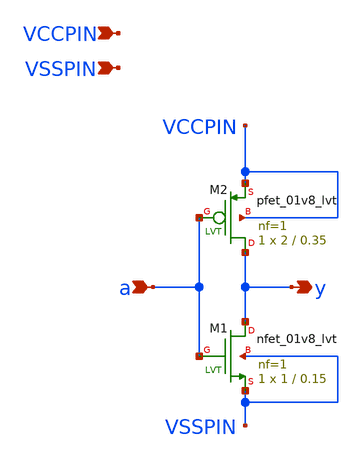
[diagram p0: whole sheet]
** sch_path: xschem/lvtnot.sch
**.subckt lvtnot y a VCCPIN VSSPIN
*.opin y
*.ipin a
*.ipin VCCPIN
*.ipin VSSPIN
XM2 y a VCCPIN VCCPIN sky130_fd_pr__pfet_01v8_lvt L=0.35 W=2 nf=1 ad='int((1 + 1)/2) * 2 / 1 * 0.29'
+ as='int((1 + 2)/2) * 2 / 1 * 0.29' pd='2*int((1 + 1)/2) * (2 / 1 + 0.29)' ps='2*int((1 + 2)/2) * (2 / 1 + 0.29)'
+ nrd='0.29 / 2 ' nrs='0.29 / 2 ' sa=0 sb=0 sd=0 mult=1 m=1
XM1 y a VSSPIN VSSPIN sky130_fd_pr__nfet_01v8_lvt L=0.15 W=1 nf=1 ad='int((1 + 1)/2) * 1 / 1 * 0.29'
+ as='int((1 + 2)/2) * 1 / 1 * 0.29' pd='2*int((1 + 1)/2) * (1 / 1 + 0.29)' ps='2*int((1 + 2)/2) * (1 / 1 + 0.29)'
+ nrd='0.29 / 1 ' nrs='0.29 / 1 ' sa=0 sb=0 sd=0 mult=1 m=1
**.ends
.end
